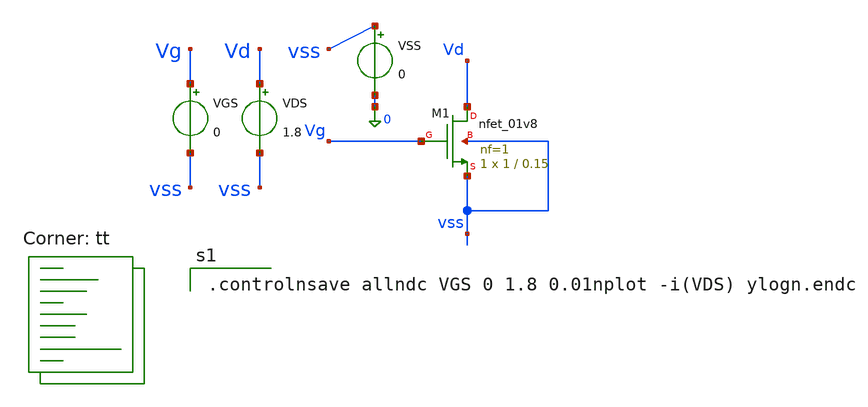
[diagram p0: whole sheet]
** sch_path: a0_device_char/prob01_ekv.sch
**.subckt prob01_ekv
XM1 Vd Vg vss vss sky130_fd_pr__nfet_01v8 L=0.15 W=1 nf=1 ad='int((1 + 1)/2) * 1 / 1 * 0.29' as='int((1 + 2)/2) * 1 / 1 * 0.29'
+ pd='2*int((1 + 1)/2) * (1 / 1 + 0.29)' ps='2*int((1 + 2)/2) * (1 / 1 + 0.29)' nrd='0.29 / 1 ' nrs='0.29 / 1 '
+ sa=0 sb=0 sd=0 mult=1 m=1
VGS Vg vss 0
VDS Vd vss 1.8
VSS vss 0 0
**** begin user architecture code
.lib $::SKYWATER_MODELS/sky130.lib.spice tt

.controlnsave allndc VGS 0 1.8 0.01nplot -i(VDS) ylogn.endc

**** end user architecture code
**.ends
.end
